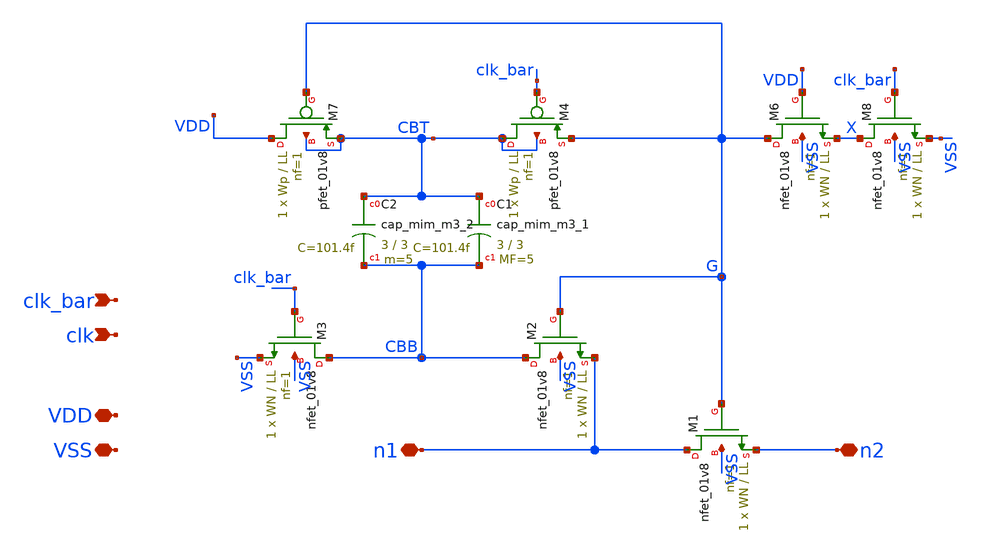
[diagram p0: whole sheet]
** sch_path: xschem/lib/Analog/Bootstrap_Switch.sch
**.subckt Bootstrap_Switch n2 n1 VDD VSS clk_bar clk
*.iopin n2
*.iopin n1
*.iopin VDD
*.iopin VSS
*.ipin clk_bar
*.ipin clk
XM1 n1 G n2 VSS sky130_fd_pr__nfet_01v8 L=LL W=WN nf=1 ad='int((1 + 1)/2) * WN / 1 * 0.29' as='int((1 + 2)/2) * WN / 1 * 0.29'
+ pd='2*int((1 + 1)/2) * (WN / 1 + 0.29)' ps='2*int((1 + 2)/2) * (WN / 1 + 0.29)' nrd='0.29 / WN ' nrs='0.29 / WN '
+ sa=0 sb=0 sd=0 mult=1 m=1
XM2 CBB G n1 VSS sky130_fd_pr__nfet_01v8 L=LL W=WN nf=1 ad='int((1 + 1)/2) * WN / 1 * 0.29' as='int((1 + 2)/2) * WN / 1 * 0.29'
+ pd='2*int((1 + 1)/2) * (WN / 1 + 0.29)' ps='2*int((1 + 2)/2) * (WN / 1 + 0.29)' nrd='0.29 / WN ' nrs='0.29 / WN '
+ sa=0 sb=0 sd=0 mult=1 m=1
XC1 CBT CBB sky130_fd_pr__cap_mim_m3_1 W=3 L=3 MF=5 m=5
XC2 CBT CBB sky130_fd_pr__cap_mim_m3_2 W=3 L=3 MF=5 m=5
XM3 CBB clk_bar VSS VSS sky130_fd_pr__nfet_01v8 L=LL W=WN nf=1 ad='int((1 + 1)/2) * WN / 1 * 0.29' as='int((1 + 2)/2) * WN / 1 * 0.29'
+ pd='2*int((1 + 1)/2) * (WN / 1 + 0.29)' ps='2*int((1 + 2)/2) * (WN / 1 + 0.29)' nrd='0.29 / WN ' nrs='0.29 / WN '
+ sa=0 sb=0 sd=0 mult=1 m=1
XM6 G VDD X VSS sky130_fd_pr__nfet_01v8 L=LL W=WN nf=1 ad='int((1 + 1)/2) * WN / 1 * 0.29' as='int((1 + 2)/2) * WN / 1 * 0.29'
+ pd='2*int((1 + 1)/2) * (WN / 1 + 0.29)' ps='2*int((1 + 2)/2) * (WN / 1 + 0.29)' nrd='0.29 / WN ' nrs='0.29 / WN '
+ sa=0 sb=0 sd=0 mult=1 m=1
XM7 VDD G CBT CBT sky130_fd_pr__pfet_01v8 L=LL W=Wp nf=1 ad='int((1 + 1)/2) * Wp / 1 * 0.29' as='int((1 + 2)/2) * Wp / 1 * 0.29'
+ pd='2*int((1 + 1)/2) * (Wp / 1 + 0.29)' ps='2*int((1 + 2)/2) * (Wp / 1 + 0.29)' nrd='0.29 / Wp ' nrs='0.29 / Wp '
+ sa=0 sb=0 sd=0 mult=1 m=1
XM8 X clk_bar VSS VSS sky130_fd_pr__nfet_01v8 L=LL W=WN nf=1 ad='int((1 + 1)/2) * WN / 1 * 0.29' as='int((1 + 2)/2) * WN / 1 * 0.29'
+ pd='2*int((1 + 1)/2) * (WN / 1 + 0.29)' ps='2*int((1 + 2)/2) * (WN / 1 + 0.29)' nrd='0.29 / WN ' nrs='0.29 / WN '
+ sa=0 sb=0 sd=0 mult=1 m=1
XM4 CBT clk_bar G CBT sky130_fd_pr__pfet_01v8 L=LL W=Wp nf=1 ad='int((1 + 1)/2) * Wp / 1 * 0.29' as='int((1 + 2)/2) * Wp / 1 * 0.29'
+ pd='2*int((1 + 1)/2) * (Wp / 1 + 0.29)' ps='2*int((1 + 2)/2) * (Wp / 1 + 0.29)' nrd='0.29 / Wp ' nrs='0.29 / Wp '
+ sa=0 sb=0 sd=0 mult=1 m=1
**.ends
.end
